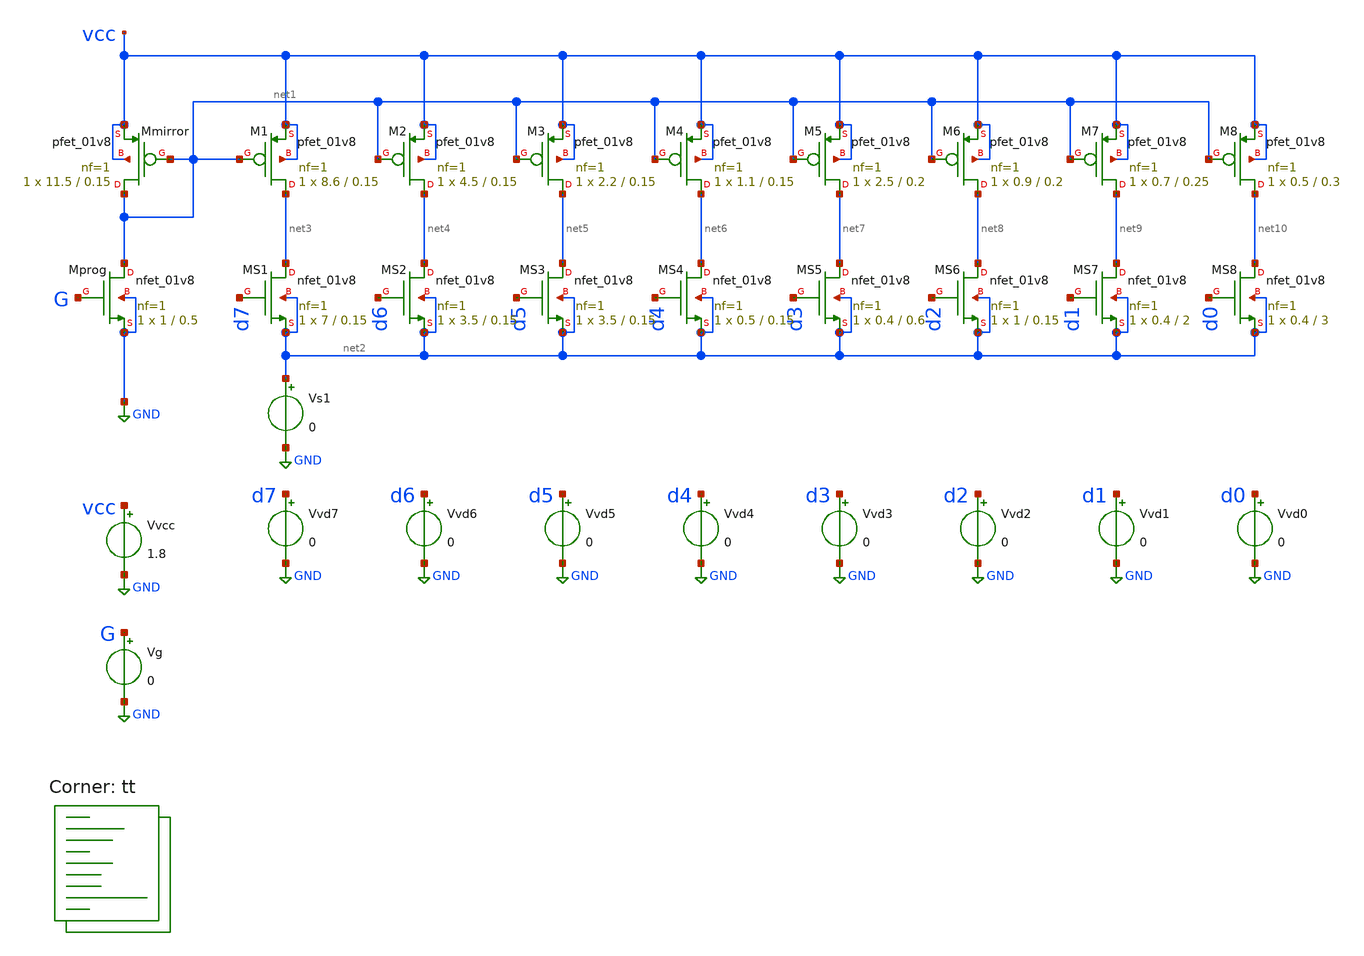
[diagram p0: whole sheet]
** sch_path: xschem/04-csdac1.sch
**.subckt 04-csdac1
Vvcc vcc GND 1.8
Vg G GND 0
XMprog net1 G GND GND sky130_fd_pr__nfet_01v8 L=0.5 W=1 nf=1 ad='int((nf+1)/2) * W/nf * 0.29' as='int((nf+2)/2) * W/nf * 0.29'
+ pd='2*int((nf+1)/2) * (W/nf + 0.29)' ps='2*int((nf+2)/2) * (W/nf + 0.29)' nrd='0.29 / W' nrs='0.29 / W'
+ sa=0 sb=0 sd=0 mult=1 m=1
XMmirror net1 net1 vcc vcc sky130_fd_pr__pfet_01v8 L=0.15 W=11.5 nf=1 ad='int((nf+1)/2) * W/nf * 0.29'
+ as='int((nf+2)/2) * W/nf * 0.29' pd='2*int((nf+1)/2) * (W/nf + 0.29)' ps='2*int((nf+2)/2) * (W/nf + 0.29)'
+ nrd='0.29 / W' nrs='0.29 / W' sa=0 sb=0 sd=0 mult=1 m=1
XM1 net3 net1 vcc vcc sky130_fd_pr__pfet_01v8 L=0.15 W=8.6 nf=1 ad='int((nf+1)/2) * W/nf * 0.29' as='int((nf+2)/2) * W/nf * 0.29'
+ pd='2*int((nf+1)/2) * (W/nf + 0.29)' ps='2*int((nf+2)/2) * (W/nf + 0.29)' nrd='0.29 / W' nrs='0.29 / W'
+ sa=0 sb=0 sd=0 mult=1 m=1
Vs1 net2 GND 0
XM2 net4 net1 vcc vcc sky130_fd_pr__pfet_01v8 L=0.15 W=4.5 nf=1 ad='int((nf+1)/2) * W/nf * 0.29' as='int((nf+2)/2) * W/nf * 0.29'
+ pd='2*int((nf+1)/2) * (W/nf + 0.29)' ps='2*int((nf+2)/2) * (W/nf + 0.29)' nrd='0.29 / W' nrs='0.29 / W'
+ sa=0 sb=0 sd=0 mult=1 m=1
XM3 net5 net1 vcc vcc sky130_fd_pr__pfet_01v8 L=0.15 W=2.2 nf=1 ad='int((nf+1)/2) * W/nf * 0.29' as='int((nf+2)/2) * W/nf * 0.29'
+ pd='2*int((nf+1)/2) * (W/nf + 0.29)' ps='2*int((nf+2)/2) * (W/nf + 0.29)' nrd='0.29 / W' nrs='0.29 / W'
+ sa=0 sb=0 sd=0 mult=1 m=1
XM4 net6 net1 vcc vcc sky130_fd_pr__pfet_01v8 L=0.15 W=1.1 nf=1 ad='int((nf+1)/2) * W/nf * 0.29' as='int((nf+2)/2) * W/nf * 0.29'
+ pd='2*int((nf+1)/2) * (W/nf + 0.29)' ps='2*int((nf+2)/2) * (W/nf + 0.29)' nrd='0.29 / W' nrs='0.29 / W'
+ sa=0 sb=0 sd=0 mult=1 m=1
XM5 net7 net1 vcc vcc sky130_fd_pr__pfet_01v8 L=0.2 W=2.5 nf=1 ad='int((nf+1)/2) * W/nf * 0.29' as='int((nf+2)/2) * W/nf * 0.29'
+ pd='2*int((nf+1)/2) * (W/nf + 0.29)' ps='2*int((nf+2)/2) * (W/nf + 0.29)' nrd='0.29 / W' nrs='0.29 / W'
+ sa=0 sb=0 sd=0 mult=1 m=1
XM6 net8 net1 vcc vcc sky130_fd_pr__pfet_01v8 L=0.2 W=0.9 nf=1 ad='int((nf+1)/2) * W/nf * 0.29' as='int((nf+2)/2) * W/nf * 0.29'
+ pd='2*int((nf+1)/2) * (W/nf + 0.29)' ps='2*int((nf+2)/2) * (W/nf + 0.29)' nrd='0.29 / W' nrs='0.29 / W'
+ sa=0 sb=0 sd=0 mult=1 m=1
XM7 net9 net1 vcc vcc sky130_fd_pr__pfet_01v8 L=0.25 W=0.7 nf=1 ad='int((nf+1)/2) * W/nf * 0.29' as='int((nf+2)/2) * W/nf * 0.29'
+ pd='2*int((nf+1)/2) * (W/nf + 0.29)' ps='2*int((nf+2)/2) * (W/nf + 0.29)' nrd='0.29 / W' nrs='0.29 / W'
+ sa=0 sb=0 sd=0 mult=1 m=1
XM8 net10 net1 vcc vcc sky130_fd_pr__pfet_01v8 L=0.3 W=0.5 nf=1 ad='int((nf+1)/2) * W/nf * 0.29' as='int((nf+2)/2) * W/nf * 0.29'
+ pd='2*int((nf+1)/2) * (W/nf + 0.29)' ps='2*int((nf+2)/2) * (W/nf + 0.29)' nrd='0.29 / W' nrs='0.29 / W'
+ sa=0 sb=0 sd=0 mult=1 m=1
XMS1 net3 d7 net2 net2 sky130_fd_pr__nfet_01v8 L=0.15 W=7 nf=1 ad='int((nf+1)/2) * W/nf * 0.29' as='int((nf+2)/2) * W/nf * 0.29'
+ pd='2*int((nf+1)/2) * (W/nf + 0.29)' ps='2*int((nf+2)/2) * (W/nf + 0.29)' nrd='0.29 / W' nrs='0.29 / W'
+ sa=0 sb=0 sd=0 mult=1 m=1
XMS2 net4 d6 net2 net2 sky130_fd_pr__nfet_01v8 L=0.15 W=3.5 nf=1 ad='int((nf+1)/2) * W/nf * 0.29' as='int((nf+2)/2) * W/nf * 0.29'
+ pd='2*int((nf+1)/2) * (W/nf + 0.29)' ps='2*int((nf+2)/2) * (W/nf + 0.29)' nrd='0.29 / W' nrs='0.29 / W'
+ sa=0 sb=0 sd=0 mult=1 m=1
XMS3 net5 d5 net2 net2 sky130_fd_pr__nfet_01v8 L=0.15 W=3.5 nf=1 ad='int((nf+1)/2) * W/nf * 0.29' as='int((nf+2)/2) * W/nf * 0.29'
+ pd='2*int((nf+1)/2) * (W/nf + 0.29)' ps='2*int((nf+2)/2) * (W/nf + 0.29)' nrd='0.29 / W' nrs='0.29 / W'
+ sa=0 sb=0 sd=0 mult=1 m=1
XMS4 net6 d4 net2 net2 sky130_fd_pr__nfet_01v8 L=0.15 W=0.5 nf=1 ad='int((nf+1)/2) * W/nf * 0.29' as='int((nf+2)/2) * W/nf * 0.29'
+ pd='2*int((nf+1)/2) * (W/nf + 0.29)' ps='2*int((nf+2)/2) * (W/nf + 0.29)' nrd='0.29 / W' nrs='0.29 / W'
+ sa=0 sb=0 sd=0 mult=1 m=1
XMS5 net7 d3 net2 net2 sky130_fd_pr__nfet_01v8 L=0.6 W=0.4 nf=1 ad='int((nf+1)/2) * W/nf * 0.29' as='int((nf+2)/2) * W/nf * 0.29'
+ pd='2*int((nf+1)/2) * (W/nf + 0.29)' ps='2*int((nf+2)/2) * (W/nf + 0.29)' nrd='0.29 / W' nrs='0.29 / W'
+ sa=0 sb=0 sd=0 mult=1 m=1
XMS6 net8 d2 net2 net2 sky130_fd_pr__nfet_01v8 L=0.15 W=1 nf=1 ad='int((nf+1)/2) * W/nf * 0.29' as='int((nf+2)/2) * W/nf * 0.29'
+ pd='2*int((nf+1)/2) * (W/nf + 0.29)' ps='2*int((nf+2)/2) * (W/nf + 0.29)' nrd='0.29 / W' nrs='0.29 / W'
+ sa=0 sb=0 sd=0 mult=1 m=1
XMS7 net9 d1 net2 net2 sky130_fd_pr__nfet_01v8 L=2 W=0.4 nf=1 ad='int((nf+1)/2) * W/nf * 0.29' as='int((nf+2)/2) * W/nf * 0.29'
+ pd='2*int((nf+1)/2) * (W/nf + 0.29)' ps='2*int((nf+2)/2) * (W/nf + 0.29)' nrd='0.29 / W' nrs='0.29 / W'
+ sa=0 sb=0 sd=0 mult=1 m=1
XMS8 net10 d0 net2 net2 sky130_fd_pr__nfet_01v8 L=3 W=0.4 nf=1 ad='int((nf+1)/2) * W/nf * 0.29' as='int((nf+2)/2) * W/nf * 0.29'
+ pd='2*int((nf+1)/2) * (W/nf + 0.29)' ps='2*int((nf+2)/2) * (W/nf + 0.29)' nrd='0.29 / W' nrs='0.29 / W'
+ sa=0 sb=0 sd=0 mult=1 m=1
Vvd0 d0 GND 0
Vvd1 d1 GND 0
Vvd2 d2 GND 0
Vvd3 d3 GND 0
Vvd4 d4 GND 0
Vvd5 d5 GND 0
Vvd6 d6 GND 0
Vvd7 d7 GND 0
**** begin user architecture code



.DC Vg 0 1.8 0.01

*.param GW     = 0.5
*.param GL     = 0.15

.options savecurrents
.control

  save all
  alter Vvd7 1.8
  run
  write 04.raw G i(Vs1)

  set appendwrite
  reset
  alter Vvd7 0
  alter Vvd6 1.8
  run
  write 04.raw G i(Vs1)

  set appendwrite
  reset
  alter Vvd6 0
  alter Vvd5 1.8
  run
  write 04.raw G i(Vs1)

  set appendwrite
  reset
  alter Vvd5 0
  alter Vvd4 1.8
  run
  write 04.raw G i(Vs1)

  set appendwrite
  reset
  alter Vvd4 0
  alter Vvd3 1.8
  run
  write 04.raw G i(Vs1)

  set appendwrite
  reset
  alter Vvd3 0
  alter Vvd2 1.8
  run
  write 04.raw G i(Vs1)

  set appendwrite
  reset
  alter Vvd2 0
  alter Vvd1 1.8
  run
  write 04.raw G i(Vs1)

  set appendwrite
  reset
  alter Vvd1 0
  alter Vvd0 1.8
  run
  write 04.raw G i(Vs1)

  * Turn all on:
  set appendwrite
  reset
  alter Vvd0 1.8
  alter Vvd1 1.8
  alter Vvd2 1.8
  alter Vvd3 1.8
  alter Vvd4 1.8
  alter Vvd5 1.8
  alter Vvd6 1.8
  alter Vvd7 1.8
  run
  write 04.raw G i(Vs1)


.endc



.lib $::SKYWATER_MODELS/sky130.lib.spice tt
**** end user architecture code
**.ends
.GLOBAL GND
.end
